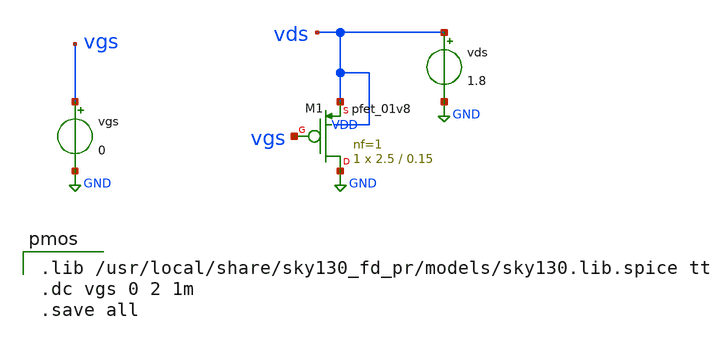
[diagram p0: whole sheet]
** sch_path: files/mos_characteristics/pmos/pmos.sch
**.subckt pmos
XM1 GND vgs vds VDD sky130_fd_pr__pfet_01v8 L=0.15 W=2.5 nf=1 ad='int((1 + 1)/2) * 2.5 / 1 * 0.29' as='int((1 + 2)/2) * 2.5 / 1 * 0.29'
+ pd='2*int((1 + 1)/2) * (2.5 / 1 + 0.29)' ps='2*int((1 + 2)/2) * (2.5 / 1 + 0.29)' nrd='0.29 / 2.5 ' nrs='0.29 / 2.5 '
+ sa=0 sb=0 sd=0 mult=1 m=1
vgs vgs GND 0
vds vds GND 1.8
**** begin user architecture code

.lib /usr/local/share/sky130_fd_pr/models/sky130.lib.spice tt
.dc vgs 0 2 1m
.save all

**** end user architecture code
**.ends
.GLOBAL GND
.end
